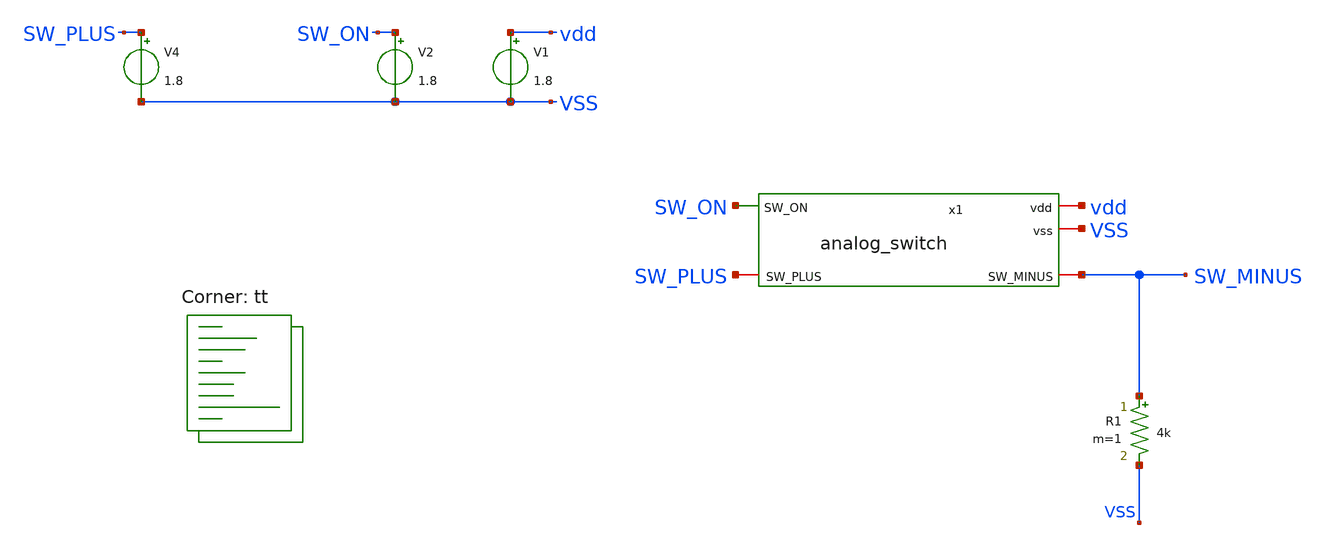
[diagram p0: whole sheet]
** sch_path: xschem/sw_tb_simple.sch
**.subckt sw_tb_simple
R1 SW_MINUS VSS 4k m=1
x1 vdd VSS SW_ON SW_PLUS SW_MINUS analog_switch
V1 vdd VSS 1.8
V2 SW_ON VSS 1.8
V4 SW_PLUS VSS 1.8
**** begin user architecture code
.lib $::SKYWATER_MODELS/sky130.lib.spice tt

.options gmin=1e-12 abstol=1e-12 reltol=1e-3
.options method=gear
.options maxord=2
R_SW_ON sw_on x1.nsw_on 1
R_LOAD sw_minus 0 1MEG
.control
.IC V(sw_on)=1.8 V(sw_plus)=1.8 V(sw_minus)=0
tran 100p 200n uic
write testbench.raw
.endc


**** end user architecture code
**.ends
.end
